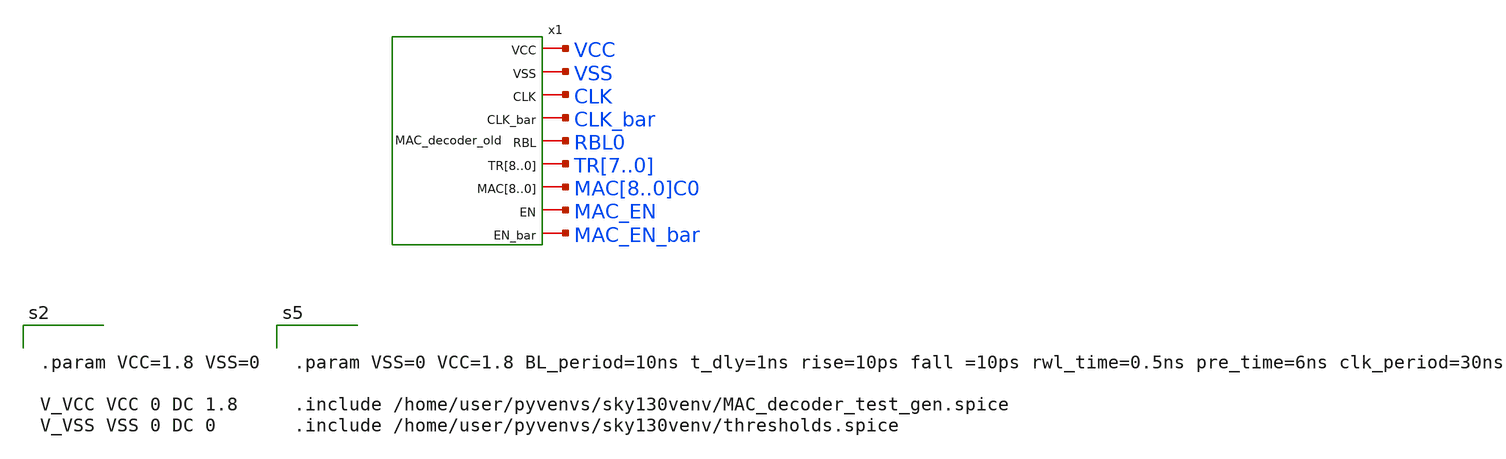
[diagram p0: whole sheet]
** sch_path: voltage_comp/MAC_decoder_old_test.sch
**.subckt MAC_decoder_old_test
x1 VCC VSS CLK CLK_bar RBL0 TR7 TR6 TR5 TR4 TR3 TR2 TR1 TR0 TR7 MAC8C0 MAC7C0 MAC6C0 MAC5C0 MAC4C0
+ MAC3C0 MAC2C0 MAC1C0 MAC0C0 MAC_EN MAC_EN_bar MAC_decoder_old
**** begin user architecture code


.param VSS=0 VCC=1.8 BL_period=10ns t_dly=1ns rise=10ps fall =10ps rwl_time=0.5ns pre_time=6ns
+ clk_period=30ns

.include /home/user/pyvenvs/sky130venv/MAC_decoder_test_gen.spice
.include /home/user/pyvenvs/sky130venv/thresholds.spice





.param VCC=1.8 VSS=0

V_VCC VCC 0 DC 1.8
V_VSS VSS 0 DC 0


**** end user architecture code
**.ends
.end
